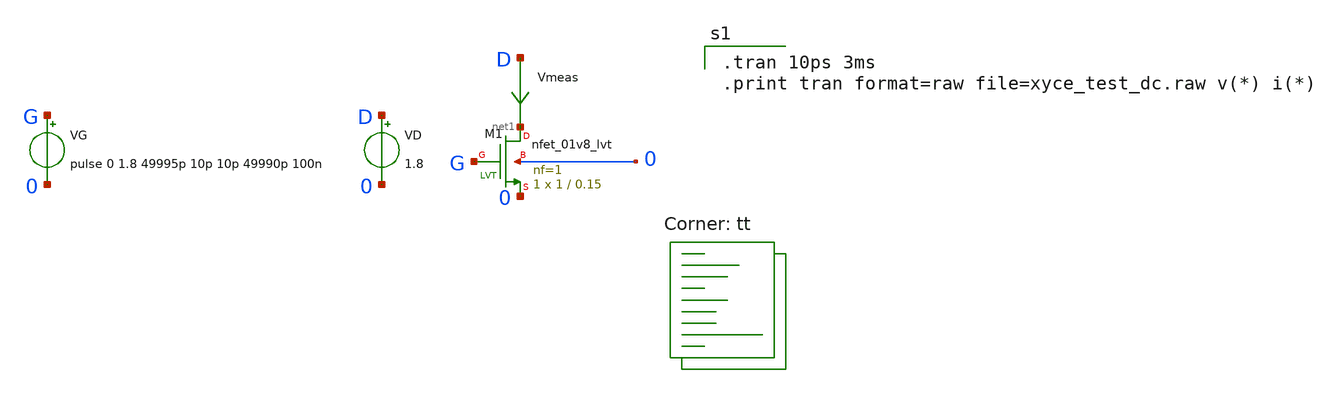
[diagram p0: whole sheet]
** sch_path: xschem/xyce_test.sch
**.subckt xyce_test
XM1 net1 G 0 0 sky130_fd_pr__nfet_01v8_lvt L=0.15 W=1 nf=1 ad='int((1 + 1)/2) * 1 / 1 * 0.29' as='int((1 + 2)/2) * 1 / 1 * 0.29'
+ pd='2*int((1 + 1)/2) * (1 / 1 + 0.29)' ps='2*int((1 + 2)/2) * (1 / 1 + 0.29)' nrd='0.29 / 1 ' nrs='0.29 / 1 '
+ sa=0 sb=0 sd=0 mult=1 m=1
VD D 0 1.8
Vmeas D net1 0
.save i(vmeas)
VG G 0 pulse 0 1.8 49995p 10p 10p 49990p 100n
**** begin user architecture code
.lib $::SKYWATER_MODELS/sky130.lib.spice tt

.tran 10ps 3ms
.print tran format=raw file=xyce_test_dc.raw v(*) i(*)

**** end user architecture code
**.ends
.end
